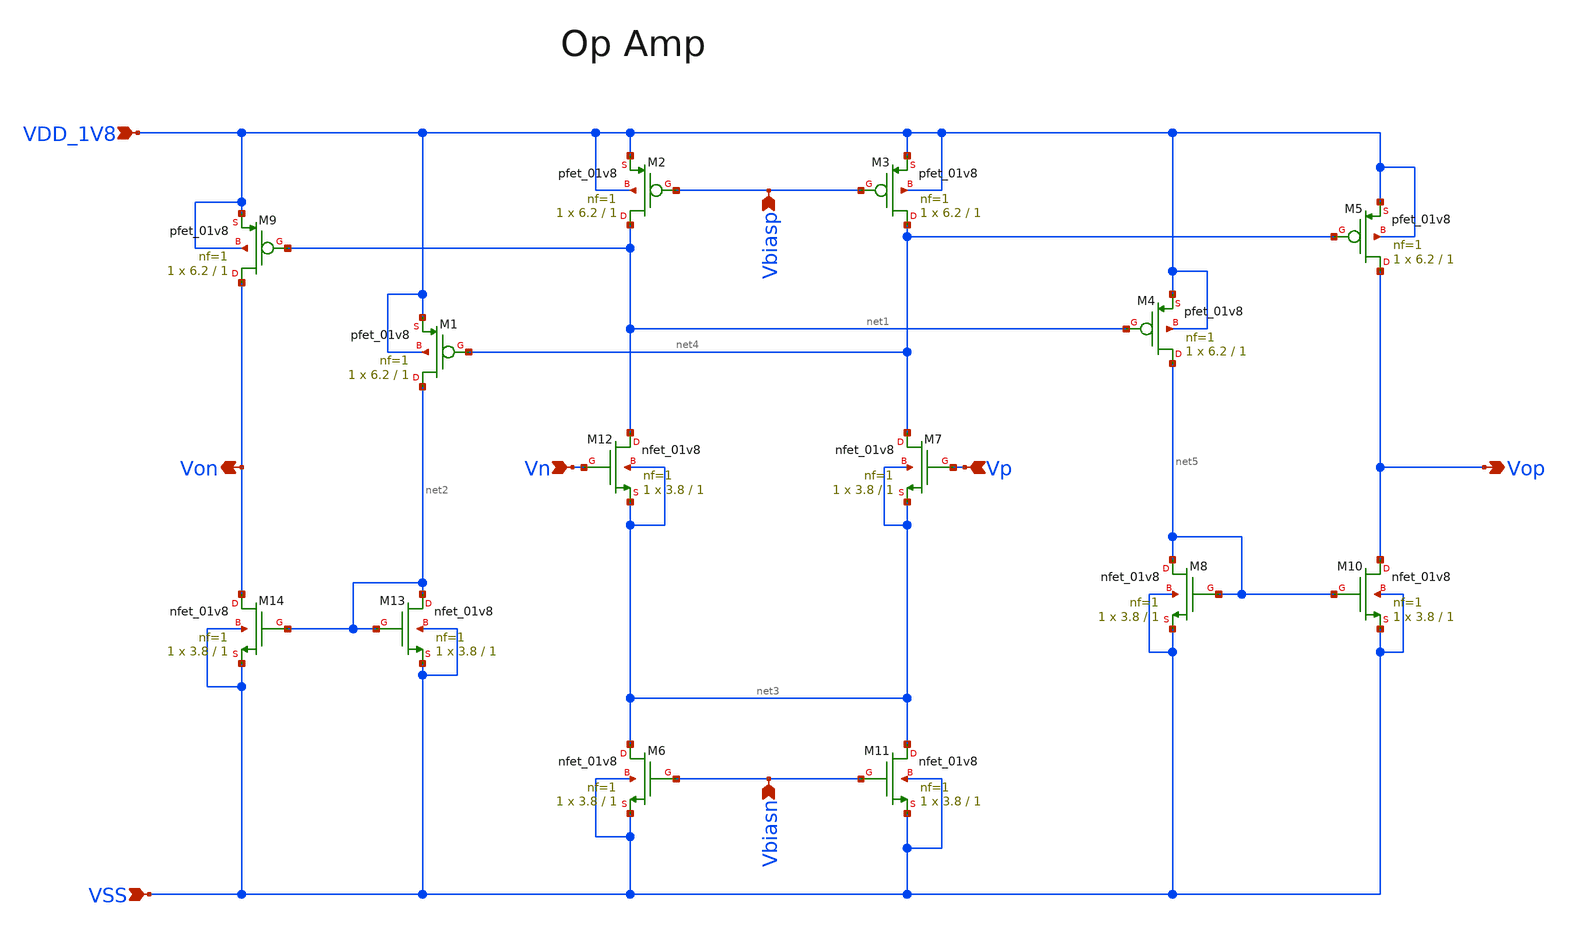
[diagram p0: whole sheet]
** sch_path: design/CNR_GR06_SKY130NM/CNR_GR06_op_amp.sch
**.subckt CNR_GR06_op_amp VDD_1V8 VSS Vop Vn Vp Vbiasp Vbiasn Von
*.ipin VDD_1V8
*.ipin VSS
*.opin Vop
*.ipin Vn
*.ipin Vp
*.ipin Vbiasp
*.ipin Vbiasn
*.opin Von
XM9 Von net1 VDD_1V8 VDD_1V8 sky130_fd_pr__pfet_01v8 L=1 W=6.2 nf=1 ad='int((nf+1)/2) * W/nf * 0.29'
+ as='int((nf+2)/2) * W/nf * 0.29' pd='2*int((nf+1)/2) * (W/nf + 0.29)' ps='2*int((nf+2)/2) * (W/nf + 0.29)'
+ nrd='0.29 / W' nrs='0.29 / W' sa=0 sb=0 sd=0 mult=1 m=1
XM14 Von net2 VSS VSS sky130_fd_pr__nfet_01v8 L=1 W=3.8 nf=1 ad='int((nf+1)/2) * W/nf * 0.29' as='int((nf+2)/2) * W/nf * 0.29'
+ pd='2*int((nf+1)/2) * (W/nf + 0.29)' ps='2*int((nf+2)/2) * (W/nf + 0.29)' nrd='0.29 / W' nrs='0.29 / W'
+ sa=0 sb=0 sd=0 mult=1 m=1
XM1 net2 net4 VDD_1V8 VDD_1V8 sky130_fd_pr__pfet_01v8 L=1 W=6.2 nf=1 ad='int((nf+1)/2) * W/nf * 0.29'
+ as='int((nf+2)/2) * W/nf * 0.29' pd='2*int((nf+1)/2) * (W/nf + 0.29)' ps='2*int((nf+2)/2) * (W/nf + 0.29)'
+ nrd='0.29 / W' nrs='0.29 / W' sa=0 sb=0 sd=0 mult=1 m=1
XM2 net1 Vbiasp VDD_1V8 VDD_1V8 sky130_fd_pr__pfet_01v8 L=1 W=6.2 nf=1 ad='int((nf+1)/2) * W/nf * 0.29'
+ as='int((nf+2)/2) * W/nf * 0.29' pd='2*int((nf+1)/2) * (W/nf + 0.29)' ps='2*int((nf+2)/2) * (W/nf + 0.29)'
+ nrd='0.29 / W' nrs='0.29 / W' sa=0 sb=0 sd=0 mult=1 m=1
XM3 net4 Vbiasp VDD_1V8 VDD_1V8 sky130_fd_pr__pfet_01v8 L=1 W=6.2 nf=1 ad='int((nf+1)/2) * W/nf * 0.29'
+ as='int((nf+2)/2) * W/nf * 0.29' pd='2*int((nf+1)/2) * (W/nf + 0.29)' ps='2*int((nf+2)/2) * (W/nf + 0.29)'
+ nrd='0.29 / W' nrs='0.29 / W' sa=0 sb=0 sd=0 mult=1 m=1
XM4 net5 net1 VDD_1V8 VDD_1V8 sky130_fd_pr__pfet_01v8 L=1 W=6.2 nf=1 ad='int((nf+1)/2) * W/nf * 0.29'
+ as='int((nf+2)/2) * W/nf * 0.29' pd='2*int((nf+1)/2) * (W/nf + 0.29)' ps='2*int((nf+2)/2) * (W/nf + 0.29)'
+ nrd='0.29 / W' nrs='0.29 / W' sa=0 sb=0 sd=0 mult=1 m=1
XM5 Vop net4 VDD_1V8 VDD_1V8 sky130_fd_pr__pfet_01v8 L=1 W=6.2 nf=1 ad='int((nf+1)/2) * W/nf * 0.29'
+ as='int((nf+2)/2) * W/nf * 0.29' pd='2*int((nf+1)/2) * (W/nf + 0.29)' ps='2*int((nf+2)/2) * (W/nf + 0.29)'
+ nrd='0.29 / W' nrs='0.29 / W' sa=0 sb=0 sd=0 mult=1 m=1
XM6 net3 Vbiasn VSS VSS sky130_fd_pr__nfet_01v8 L=1 W=3.8 nf=1 ad='int((nf+1)/2) * W/nf * 0.29' as='int((nf+2)/2) * W/nf * 0.29'
+ pd='2*int((nf+1)/2) * (W/nf + 0.29)' ps='2*int((nf+2)/2) * (W/nf + 0.29)' nrd='0.29 / W' nrs='0.29 / W'
+ sa=0 sb=0 sd=0 mult=1 m=1
XM7 net4 Vp net3 net3 sky130_fd_pr__nfet_01v8 L=1 W=3.8 nf=1 ad='int((nf+1)/2) * W/nf * 0.29' as='int((nf+2)/2) * W/nf * 0.29'
+ pd='2*int((nf+1)/2) * (W/nf + 0.29)' ps='2*int((nf+2)/2) * (W/nf + 0.29)' nrd='0.29 / W' nrs='0.29 / W'
+ sa=0 sb=0 sd=0 mult=1 m=1
XM8 net5 net5 VSS VSS sky130_fd_pr__nfet_01v8 L=1 W=3.8 nf=1 ad='int((nf+1)/2) * W/nf * 0.29' as='int((nf+2)/2) * W/nf * 0.29'
+ pd='2*int((nf+1)/2) * (W/nf + 0.29)' ps='2*int((nf+2)/2) * (W/nf + 0.29)' nrd='0.29 / W' nrs='0.29 / W'
+ sa=0 sb=0 sd=0 mult=1 m=1
XM10 Vop net5 VSS VSS sky130_fd_pr__nfet_01v8 L=1 W=3.8 nf=1 ad='int((nf+1)/2) * W/nf * 0.29' as='int((nf+2)/2) * W/nf * 0.29'
+ pd='2*int((nf+1)/2) * (W/nf + 0.29)' ps='2*int((nf+2)/2) * (W/nf + 0.29)' nrd='0.29 / W' nrs='0.29 / W'
+ sa=0 sb=0 sd=0 mult=1 m=1
XM11 net3 Vbiasn VSS VSS sky130_fd_pr__nfet_01v8 L=1 W=3.8 nf=1 ad='int((nf+1)/2) * W/nf * 0.29' as='int((nf+2)/2) * W/nf * 0.29'
+ pd='2*int((nf+1)/2) * (W/nf + 0.29)' ps='2*int((nf+2)/2) * (W/nf + 0.29)' nrd='0.29 / W' nrs='0.29 / W'
+ sa=0 sb=0 sd=0 mult=1 m=1
XM12 net1 Vn net3 net3 sky130_fd_pr__nfet_01v8 L=1 W=3.8 nf=1 ad='int((nf+1)/2) * W/nf * 0.29' as='int((nf+2)/2) * W/nf * 0.29'
+ pd='2*int((nf+1)/2) * (W/nf + 0.29)' ps='2*int((nf+2)/2) * (W/nf + 0.29)' nrd='0.29 / W' nrs='0.29 / W'
+ sa=0 sb=0 sd=0 mult=1 m=1
XM13 net2 net2 VSS VSS sky130_fd_pr__nfet_01v8 L=1 W=3.8 nf=1 ad='int((nf+1)/2) * W/nf * 0.29' as='int((nf+2)/2) * W/nf * 0.29'
+ pd='2*int((nf+1)/2) * (W/nf + 0.29)' ps='2*int((nf+2)/2) * (W/nf + 0.29)' nrd='0.29 / W' nrs='0.29 / W'
+ sa=0 sb=0 sd=0 mult=1 m=1
**.ends
.end
